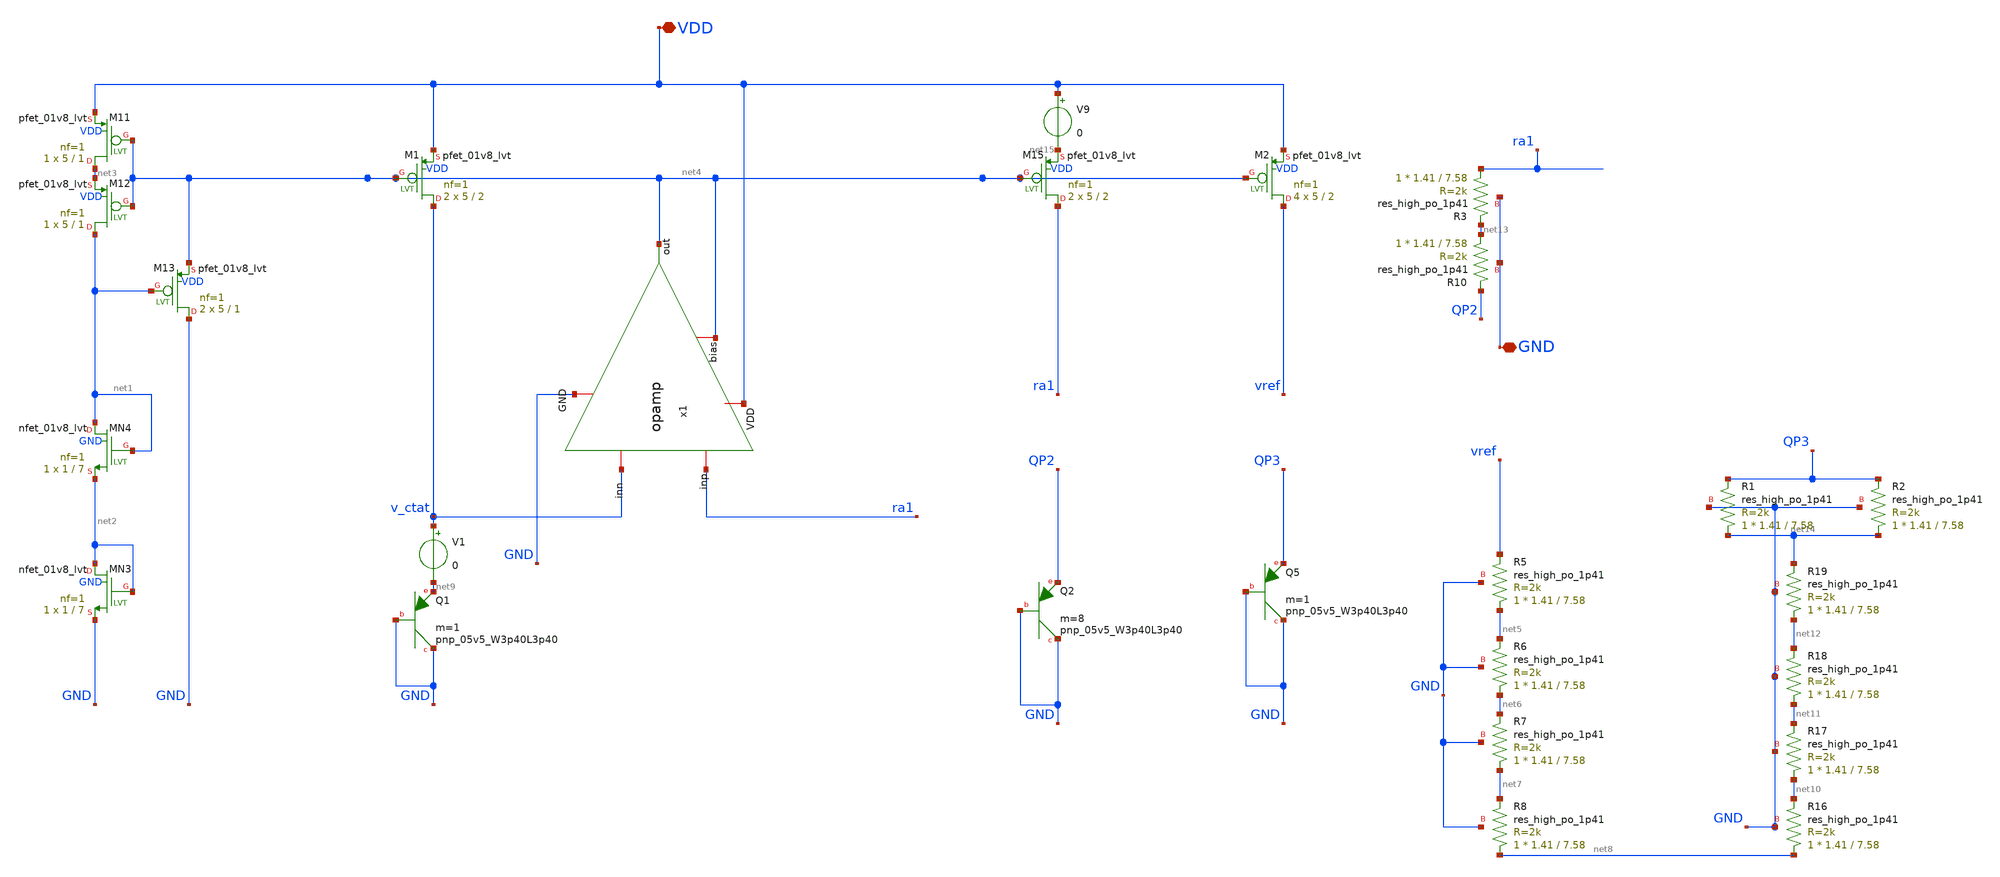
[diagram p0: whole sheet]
** sch_path: NES-2026/STDCELLS/xschem/BGR_opamp_sc.sch
**.subckt BGR_opamp_sc VDD GND
*.iopin VDD
*.iopin GND
XM11 net3 net4 VDD VDD sky130_fd_pr__pfet_01v8_lvt L=1 W=5 nf=1 ad='int((1 + 1)/2) * 5 / 1 * 0.29' as='int((1 + 2)/2) * 5 / 1 * 0.29'
+ pd='2*int((1 + 1)/2) * (5 / 1 + 0.29)' ps='2*int((1 + 2)/2) * (5 / 1 + 0.29)' nrd='0.29 / 5 ' nrs='0.29 / 5 '
+ sa=0 sb=0 sd=0 mult=1 m=1
XM12 net1 net4 net3 VDD sky130_fd_pr__pfet_01v8_lvt L=1 W=5 nf=1 ad='int((1 + 1)/2) * 5 / 1 * 0.29' as='int((1 + 2)/2) * 5 / 1 * 0.29'
+ pd='2*int((1 + 1)/2) * (5 / 1 + 0.29)' ps='2*int((1 + 2)/2) * (5 / 1 + 0.29)' nrd='0.29 / 5 ' nrs='0.29 / 5 '
+ sa=0 sb=0 sd=0 mult=1 m=1
XM13 GND net1 net4 VDD sky130_fd_pr__pfet_01v8_lvt L=1 W=5 nf=1 ad='int((1 + 1)/2) * 5 / 1 * 0.29' as='int((1 + 2)/2) * 5 / 1 * 0.29'
+ pd='2*int((1 + 1)/2) * (5 / 1 + 0.29)' ps='2*int((1 + 2)/2) * (5 / 1 + 0.29)' nrd='0.29 / 5 ' nrs='0.29 / 5 '
+ sa=0 sb=0 sd=0 mult=2 m=2
XMN3 net2 net2 GND GND sky130_fd_pr__nfet_01v8_lvt L=7 W=1 nf=1 ad='int((1 + 1)/2) * 1 / 1 * 0.29' as='int((1 + 2)/2) * 1 / 1 * 0.29'
+ pd='2*int((1 + 1)/2) * (1 / 1 + 0.29)' ps='2*int((1 + 2)/2) * (1 / 1 + 0.29)' nrd='0.29 / 1 ' nrs='0.29 / 1 '
+ sa=0 sb=0 sd=0 mult=1 m=1
XMN4 net1 net1 net2 GND sky130_fd_pr__nfet_01v8_lvt L=7 W=1 nf=1 ad='int((1 + 1)/2) * 1 / 1 * 0.29' as='int((1 + 2)/2) * 1 / 1 * 0.29'
+ pd='2*int((1 + 1)/2) * (1 / 1 + 0.29)' ps='2*int((1 + 2)/2) * (1 / 1 + 0.29)' nrd='0.29 / 1 ' nrs='0.29 / 1 '
+ sa=0 sb=0 sd=0 mult=1 m=1
XM15 ra1 net4 net15 VDD sky130_fd_pr__pfet_01v8_lvt L=2 W=5 nf=1 ad='int((1 + 1)/2) * 5 / 1 * 0.29' as='int((1 + 2)/2) * 5 / 1 * 0.29'
+ pd='2*int((1 + 1)/2) * (5 / 1 + 0.29)' ps='2*int((1 + 2)/2) * (5 / 1 + 0.29)' nrd='0.29 / 5 ' nrs='0.29 / 5 '
+ sa=0 sb=0 sd=0 mult=2 m=2
XR3 ra1 net13 GND sky130_fd_pr__res_high_po_1p41 L=7.58 mult=1 m=1
XQ2 GND GND QP2 sky130_fd_pr__pnp_05v5_W3p40L3p40 m=8
XR5 net5 vref GND sky130_fd_pr__res_high_po_1p41 L=7.58 mult=1 m=1
XR6 net6 net5 GND sky130_fd_pr__res_high_po_1p41 L=7.58 mult=1 m=1
XR7 net7 net6 GND sky130_fd_pr__res_high_po_1p41 L=7.58 mult=1 m=1
XM2 vref net4 VDD VDD sky130_fd_pr__pfet_01v8_lvt L=2 W=5 nf=1 ad='int((1 + 1)/2) * 5 / 1 * 0.29' as='int((1 + 2)/2) * 5 / 1 * 0.29'
+ pd='2*int((1 + 1)/2) * (5 / 1 + 0.29)' ps='2*int((1 + 2)/2) * (5 / 1 + 0.29)' nrd='0.29 / 5 ' nrs='0.29 / 5 '
+ sa=0 sb=0 sd=0 mult=4 m=4
XQ5 GND GND QP3 sky130_fd_pr__pnp_05v5_W3p40L3p40 m=1
V9 VDD net15 0
x1 VDD net4 ra1 net4 v_ctat GND opamp
XQ1 GND GND net9 sky130_fd_pr__pnp_05v5_W3p40L3p40 m=1
XR10 net13 QP2 GND sky130_fd_pr__res_high_po_1p41 L=7.58 mult=1 m=1
XR8 net8 net7 GND sky130_fd_pr__res_high_po_1p41 L=7.58 mult=1 m=1
V1 v_ctat net9 0
XM1 v_ctat net4 VDD VDD sky130_fd_pr__pfet_01v8_lvt L=2 W=5 nf=1 ad='int((1 + 1)/2) * 5 / 1 * 0.29' as='int((1 + 2)/2) * 5 / 1 * 0.29'
+ pd='2*int((1 + 1)/2) * (5 / 1 + 0.29)' ps='2*int((1 + 2)/2) * (5 / 1 + 0.29)' nrd='0.29 / 5 ' nrs='0.29 / 5 '
+ sa=0 sb=0 sd=0 mult=2 m=2
XR16 net8 net10 GND sky130_fd_pr__res_high_po_1p41 L=7.58 mult=1 m=1
XR17 net10 net11 GND sky130_fd_pr__res_high_po_1p41 L=7.58 mult=1 m=1
XR18 net11 net12 GND sky130_fd_pr__res_high_po_1p41 L=7.58 mult=1 m=1
XR19 net12 net14 GND sky130_fd_pr__res_high_po_1p41 L=7.58 mult=1 m=1
XR1 net14 QP3 GND sky130_fd_pr__res_high_po_1p41 L=7.58 mult=1 m=1
XR2 net14 QP3 GND sky130_fd_pr__res_high_po_1p41 L=7.58 mult=1 m=1
**** begin user architecture code

.title BGR_opamp
.lib /home/somya/share/pdk/sky130A/libs.tech/ngspice/sky130.lib.spice tt
.temp 27
.global VDD GND
*.dc vin 0 1.8 0.01
.save all

vsup    VDD     GND     dc      2
.dc temp -40 125 5

*vsup   vdd     gnd     pulse   0       2       10n     1u      1u      1m      100u
*.tran  5n      10u

.control
run
*meas dc VREF_MIN MIN v(vref)
*meas dc VREF_NOM FIND v(vref) AT=27
plot v(vref)

plot v(v_ctat) v(vref) - v(QP3)
*plot v(QP2)
*plot v(ra1) - v(QP2)

*plot i(V1) i(V9)

*PLOT v(M7gate) v(ra1) v(QP2)
*plot vid1#branch vid2#branch vid3#branch vid4#branch vid5#branch
*plot i(V1) i(V2) i(V3) i(V8) i(V9)
.endc
.end


**** end user architecture code
**.ends

* expanding   symbol:  opamp.sym # of pins=6
** sym_path: NES-2026/STDCELLS/xschem/opamp.sym
** sch_path: NES-2026/STDCELLS/xschem/opamp.sch
.subckt opamp VDD bias inp out inn GND
*.iopin VDD
*.iopin GND
*.opin out
*.iopin inn
*.iopin inp
*.iopin bias
XM1 net1 bias net10 VDD sky130_fd_pr__pfet_01v8_lvt L=2 W=5 nf=1 ad='int((1 + 1)/2) * 5 / 1 * 0.29' as='int((1 + 2)/2) * 5 / 1 * 0.29'
+ pd='2*int((1 + 1)/2) * (5 / 1 + 0.29)' ps='2*int((1 + 2)/2) * (5 / 1 + 0.29)' nrd='0.29 / 5 ' nrs='0.29 / 5 '
+ sa=0 sb=0 sd=0 mult=2 m=2
XM3 out net2 net11 VDD sky130_fd_pr__pfet_01v8_lvt L=2 W=5 nf=1 ad='int((1 + 1)/2) * 5 / 1 * 0.29' as='int((1 + 2)/2) * 5 / 1 * 0.29'
+ pd='2*int((1 + 1)/2) * (5 / 1 + 0.29)' ps='2*int((1 + 2)/2) * (5 / 1 + 0.29)' nrd='0.29 / 5 ' nrs='0.29 / 5 '
+ sa=0 sb=0 sd=0 mult=1 m=1
XM4 net2 net2 net9 VDD sky130_fd_pr__pfet_01v8_lvt L=2 W=5 nf=1 ad='int((1 + 1)/2) * 5 / 1 * 0.29' as='int((1 + 2)/2) * 5 / 1 * 0.29'
+ pd='2*int((1 + 1)/2) * (5 / 1 + 0.29)' ps='2*int((1 + 2)/2) * (5 / 1 + 0.29)' nrd='0.29 / 5 ' nrs='0.29 / 5 '
+ sa=0 sb=0 sd=0 mult=1 m=1
XM5 net3 net3 net5 GND sky130_fd_pr__nfet_01v8 L=2 W=1 nf=1 ad='int((1 + 1)/2) * 1 / 1 * 0.29' as='int((1 + 2)/2) * 1 / 1 * 0.29'
+ pd='2*int((1 + 1)/2) * (1 / 1 + 0.29)' ps='2*int((1 + 2)/2) * (1 / 1 + 0.29)' nrd='0.29 / 1 ' nrs='0.29 / 1 '
+ sa=0 sb=0 sd=0 mult=2 m=2
XM6 net4 net4 net6 GND sky130_fd_pr__nfet_01v8 L=2 W=1 nf=1 ad='int((1 + 1)/2) * 1 / 1 * 0.29' as='int((1 + 2)/2) * 1 / 1 * 0.29'
+ pd='2*int((1 + 1)/2) * (1 / 1 + 0.29)' ps='2*int((1 + 2)/2) * (1 / 1 + 0.29)' nrd='0.29 / 1 ' nrs='0.29 / 1 '
+ sa=0 sb=0 sd=0 mult=2 m=2
XM7 net3 inn net1 VDD sky130_fd_pr__pfet_01v8_lvt L=2 W=5 nf=1 ad='int((1 + 1)/2) * 5 / 1 * 0.29' as='int((1 + 2)/2) * 5 / 1 * 0.29'
+ pd='2*int((1 + 1)/2) * (5 / 1 + 0.29)' ps='2*int((1 + 2)/2) * (5 / 1 + 0.29)' nrd='0.29 / 5 ' nrs='0.29 / 5 '
+ sa=0 sb=0 sd=0 mult=5 m=5
XM8 net4 inp net1 VDD sky130_fd_pr__pfet_01v8_lvt L=2 W=5 nf=1 ad='int((1 + 1)/2) * 5 / 1 * 0.29' as='int((1 + 2)/2) * 5 / 1 * 0.29'
+ pd='2*int((1 + 1)/2) * (5 / 1 + 0.29)' ps='2*int((1 + 2)/2) * (5 / 1 + 0.29)' nrd='0.29 / 5 ' nrs='0.29 / 5 '
+ sa=0 sb=0 sd=0 mult=5 m=5
XM9 out net4 net7 GND sky130_fd_pr__nfet_01v8 L=2 W=1 nf=1 ad='int((1 + 1)/2) * 1 / 1 * 0.29' as='int((1 + 2)/2) * 1 / 1 * 0.29'
+ pd='2*int((1 + 1)/2) * (1 / 1 + 0.29)' ps='2*int((1 + 2)/2) * (1 / 1 + 0.29)' nrd='0.29 / 1 ' nrs='0.29 / 1 '
+ sa=0 sb=0 sd=0 mult=2 m=2
XM10 net2 net3 net8 GND sky130_fd_pr__nfet_01v8 L=2 W=1 nf=1 ad='int((1 + 1)/2) * 1 / 1 * 0.29' as='int((1 + 2)/2) * 1 / 1 * 0.29'
+ pd='2*int((1 + 1)/2) * (1 / 1 + 0.29)' ps='2*int((1 + 2)/2) * (1 / 1 + 0.29)' nrd='0.29 / 1 ' nrs='0.29 / 1 '
+ sa=0 sb=0 sd=0 mult=2 m=2
V1 VDD net9 0
V2 VDD net10 0
V3 VDD net11 0
V4 net7 GND 0
V5 net6 GND 0
V6 net5 GND 0
V7 net8 GND 0
.ends

.end
